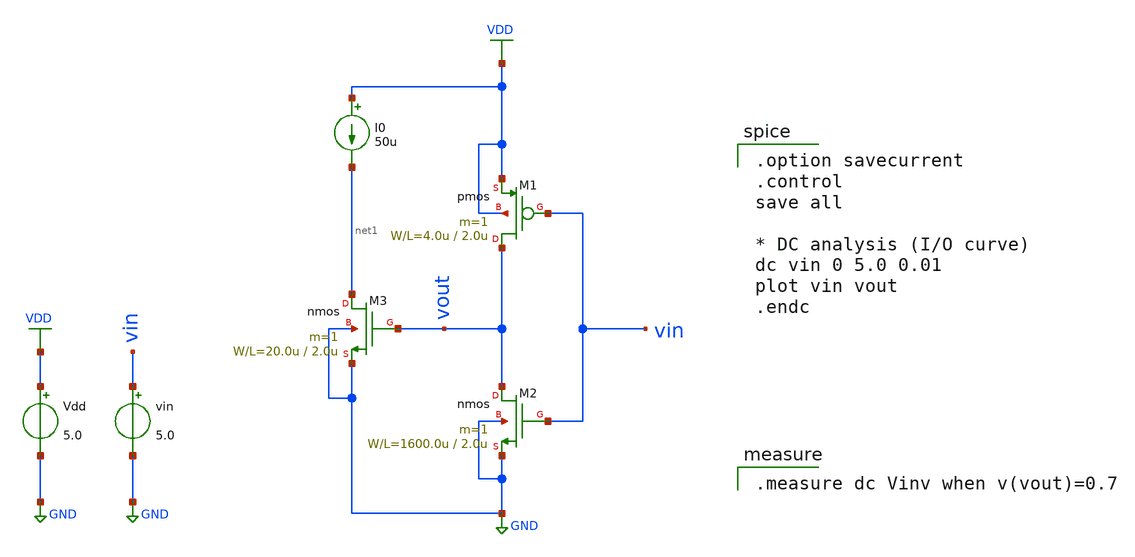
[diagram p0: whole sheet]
** sch_path: OR1/PTC06/current-source/cs_startup.sch
**.subckt cs_startup
Vdd VDD GND 5.0
vin vin GND 5.0
M1 vout vin VDD VDD pmos L=2.0u W=4.0u m=1
M2 vout vin GND GND nmos L=2.0u W=1600.0u m=1
M3 net1 vout GND GND nmos L=2.0u W=20.0u m=1
I0 VDD net1 50u
**** begin user architecture code
 .include $::LIB/mos.lib
.include $::LIB/passive.lib
.include $::LIB/diode.lib

.option savecurrent
.control
save all

* DC analysis (I/O curve)
dc vin 0 5.0 0.01
plot vin vout
.endc


.measure dc Vinv when v(vout)=0.7

**** end user architecture code
**.ends
.GLOBAL VDD
.GLOBAL GND
.end
